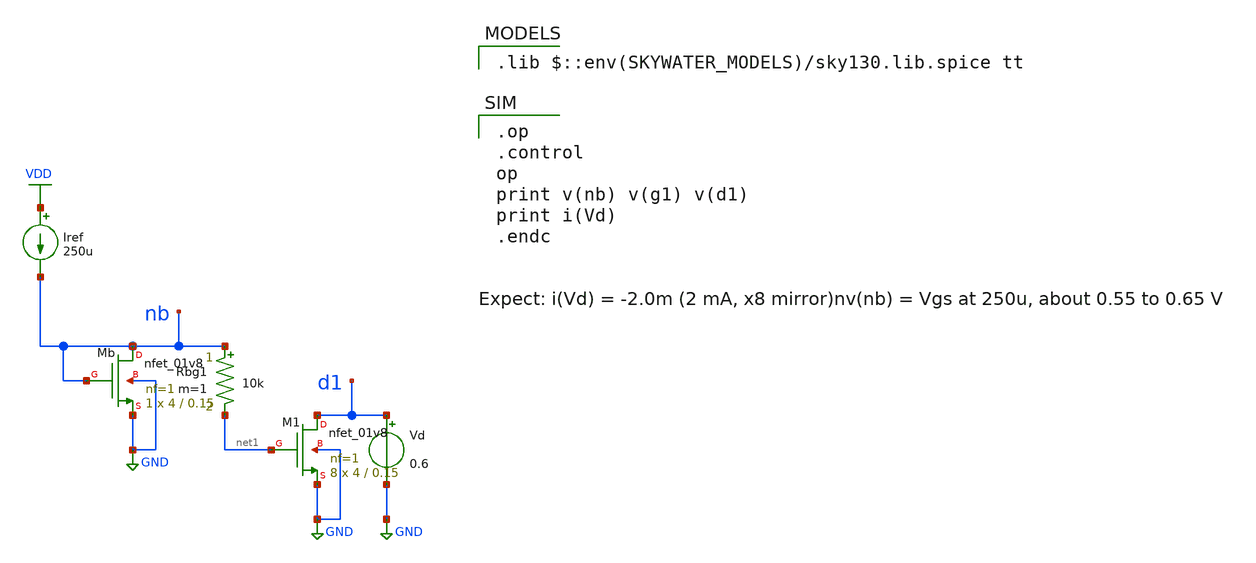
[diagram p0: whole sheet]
** sch_path: 09-sky130-gilbert-mixer-rfic/schematics/1_gm_bias.sch
**.subckt 1_gm_bias
Iref VDD nb 250u
XMb nb nb GND GND sky130_fd_pr__nfet_01v8 L=0.15 W=4 nf=1 ad='int((nf+1)/2) * W/nf * 0.29' as='int((nf+2)/2) * W/nf * 0.29'
+ pd='2*int((nf+1)/2) * (W/nf + 0.29)' ps='2*int((nf+2)/2) * (W/nf + 0.29)' nrd='0.29 / W' nrs='0.29 / W'
+ sa=0 sb=0 sd=0 mult=1 m=1
Rbg1 nb net1 10k m=1
XM1 d1 net1 GND GND sky130_fd_pr__nfet_01v8 L=0.15 W=4 nf=1 ad='int((nf+1)/2) * W/nf * 0.29' as='int((nf+2)/2) * W/nf * 0.29'
+ pd='2*int((nf+1)/2) * (W/nf + 0.29)' ps='2*int((nf+2)/2) * (W/nf + 0.29)' nrd='0.29 / W' nrs='0.29 / W'
+ sa=0 sb=0 sd=0 mult=8 m=8
Vd d1 GND 0.6
**** begin user architecture code
 .lib $::env(SKYWATER_MODELS)/sky130.lib.spice tt

.op
.control
op
print v(nb) v(g1) v(d1)
print i(Vd)
.endc

**** end user architecture code
**.ends
.GLOBAL VDD
.GLOBAL GND
.end
